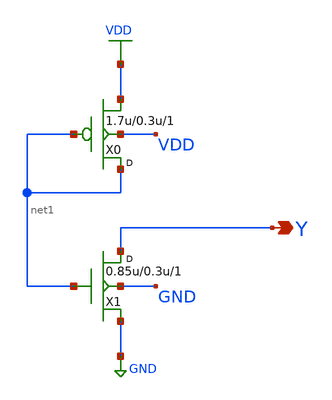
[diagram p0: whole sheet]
** sch_path: openfasoc/common/platforms/gf180mcuosu9Ttielo/gf180mcu_osu_sc_tielo.sch
**.subckt gf180mcu_osu_sc_tielo Y
*.opin Y
X0 net1 net1 VDD VDD pmos_3p3 w=1.7u l=0.3u m=1
X1 Y net1 GND GND nmos_3p3 w=0.85u l=0.3u m=1
**.ends
.GLOBAL VDD
.GLOBAL GND
.end
